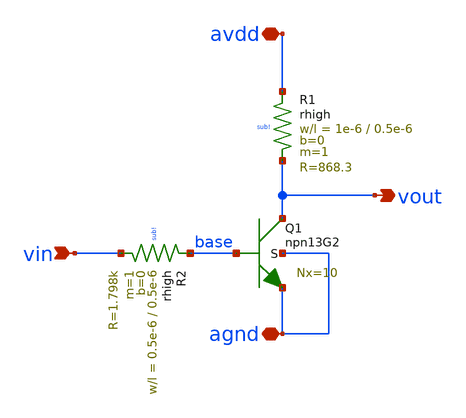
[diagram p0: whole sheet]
** sch_path: xschem/inverter.sch
**.subckt inverter avdd vin vout agnd
*.iopin avdd
*.ipin vin
*.opin vout
*.iopin agnd
XQ1 vout base agnd agnd npn13G2 Nx=10 mm_ok=1
XR1 avdd vout sub! rhigh w=1e-6 l=0.5e-6 m=1 b=0 mm_ok=1
XR2 base vin sub! rhigh w=0.5e-6 l=0.5e-6 m=1 b=0 mm_ok=1
**.ends
.end
